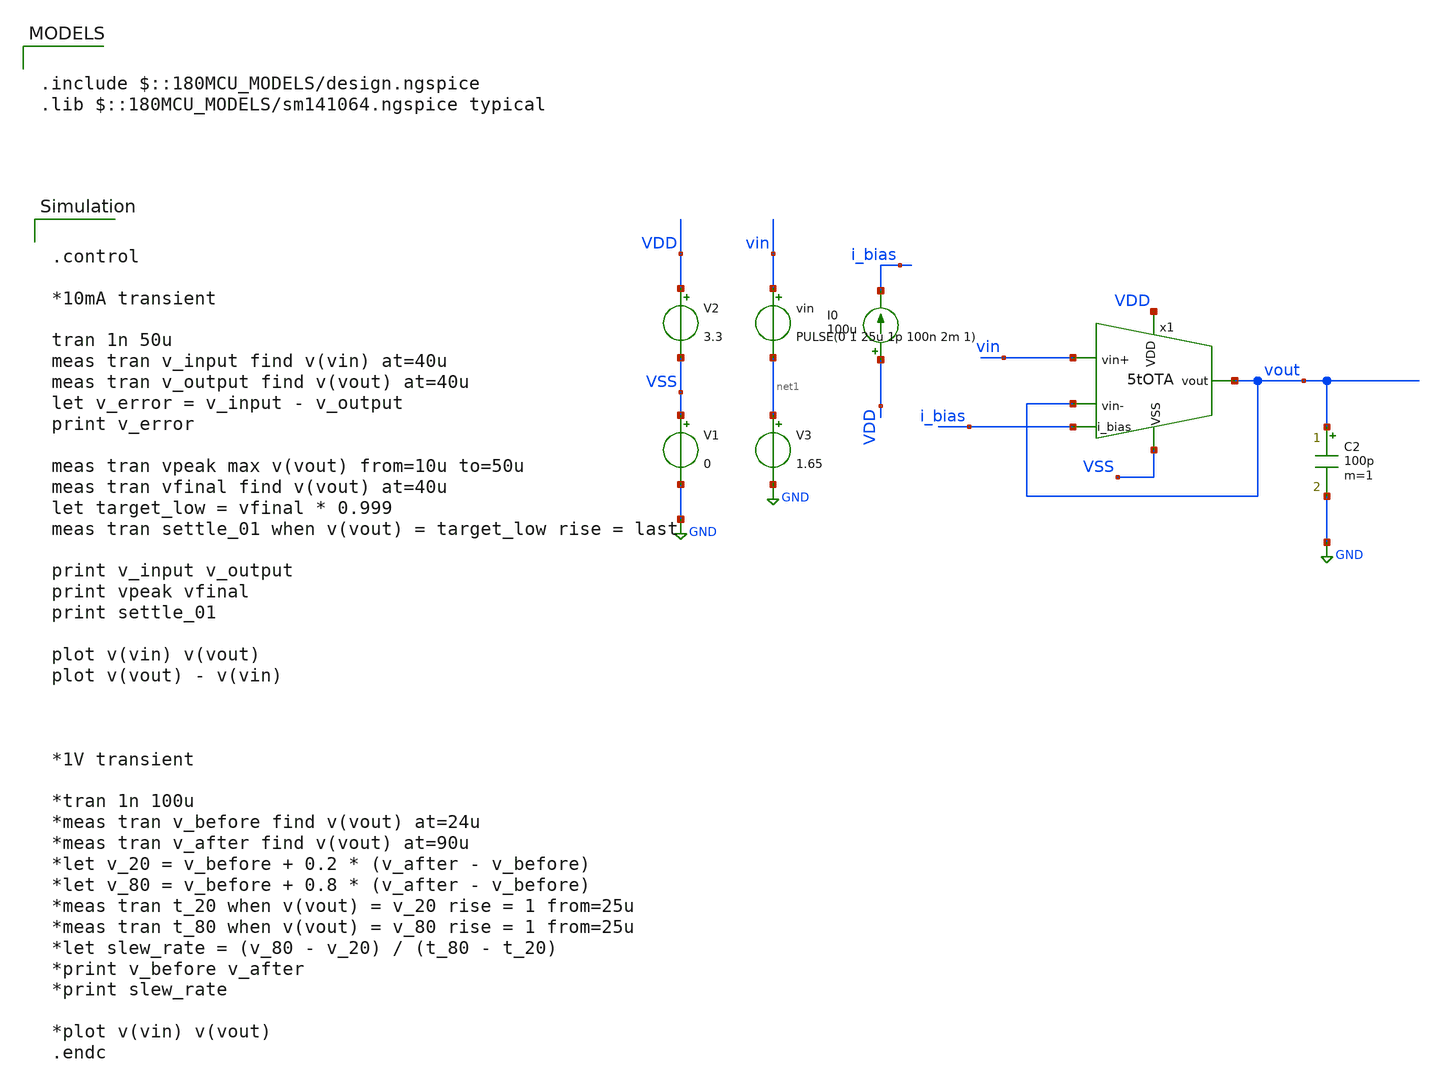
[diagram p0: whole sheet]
** sch_path: designs/5tOTA_tb_tran.sch
**.subckt 5tOTA_tb_tran
x1 VDD vout vin vout i_bias VSS 5tOTA
V1 VSS GND 0
V2 VDD VSS 3.3
I0 VDD i_bias 100u
vin vin net1 PULSE(0 1 25u 1p 100n 2m 1)
C2 vout GND 100p m=1
V3 net1 GND 1.65
**** begin user architecture code

.include $::180MCU_MODELS/design.ngspice
.lib $::180MCU_MODELS/sm141064.ngspice typical



.control

*10mA transient

tran 1n 50u
meas tran v_input find v(vin) at=40u
meas tran v_output find v(vout) at=40u
let v_error = v_input - v_output
print v_error

meas tran vpeak max v(vout) from=10u to=50u
meas tran vfinal find v(vout) at=40u
let target_low = vfinal * 0.999
meas tran settle_01 when v(vout) = target_low rise = last

print v_input v_output
print vpeak vfinal
print settle_01

plot v(vin) v(vout)
plot v(vout) - v(vin)



*1V transient

*tran 1n 100u
*meas tran v_before find v(vout) at=24u
*meas tran v_after find v(vout) at=90u
*let v_20 = v_before + 0.2 * (v_after - v_before)
*let v_80 = v_before + 0.8 * (v_after - v_before)
*meas tran t_20 when v(vout) = v_20 rise = 1 from=25u
*meas tran t_80 when v(vout) = v_80 rise = 1 from=25u
*let slew_rate = (v_80 - v_20) / (t_80 - t_20)
*print v_before v_after
*print slew_rate

*plot v(vin) v(vout)
.endc


**** end user architecture code
**.ends

* expanding   symbol:  5tOTA.sym # of pins=6
** sym_path: designs/5tOTA.sym
** sch_path: designs/5tOTA.sch
.subckt 5tOTA VDD vout vin+ vin- i_bias VSS
*.ipin VDD
*.opin vout
*.ipin i_bias
*.ipin vin+
*.ipin vin-
*.ipin VSS
XM1 net1 vin+ net2 VSS nfet_03v3 L=0.5u W=11.43u nf=1 ad='int((nf+1)/2) * W/nf * 0.18u' as='int((nf+2)/2) * W/nf * 0.18u'
+ pd='2*int((nf+1)/2) * (W/nf + 0.18u)' ps='2*int((nf+2)/2) * (W/nf + 0.18u)' nrd='0.18u / W' nrs='0.18u / W'
+ sa=0 sb=0 sd=0 m=1
XM2 vout vin- net2 VSS nfet_03v3 L=0.5u W=11.43u nf=1 ad='int((nf+1)/2) * W/nf * 0.18u' as='int((nf+2)/2) * W/nf * 0.18u'
+ pd='2*int((nf+1)/2) * (W/nf + 0.18u)' ps='2*int((nf+2)/2) * (W/nf + 0.18u)' nrd='0.18u / W' nrs='0.18u / W'
+ sa=0 sb=0 sd=0 m=1
XM3 net1 net1 VDD VDD pfet_03v3 L=0.5u W=22.86u nf=1 ad='int((nf+1)/2) * W/nf * 0.18u' as='int((nf+2)/2) * W/nf * 0.18u'
+ pd='2*int((nf+1)/2) * (W/nf + 0.18u)' ps='2*int((nf+2)/2) * (W/nf + 0.18u)' nrd='0.18u / W' nrs='0.18u / W'
+ sa=0 sb=0 sd=0 m=1
XM4 vout net1 VDD VDD pfet_03v3 L=0.5u W=22.86u nf=1 ad='int((nf+1)/2) * W/nf * 0.18u' as='int((nf+2)/2) * W/nf * 0.18u'
+ pd='2*int((nf+1)/2) * (W/nf + 0.18u)' ps='2*int((nf+2)/2) * (W/nf + 0.18u)' nrd='0.18u / W' nrs='0.18u / W'
+ sa=0 sb=0 sd=0 m=1
XM5 net2 i_bias VSS VSS nfet_03v3 L=0.5u W=22.86u nf=1 ad='int((nf+1)/2) * W/nf * 0.18u' as='int((nf+2)/2) * W/nf * 0.18u'
+ pd='2*int((nf+1)/2) * (W/nf + 0.18u)' ps='2*int((nf+2)/2) * (W/nf + 0.18u)' nrd='0.18u / W' nrs='0.18u / W'
+ sa=0 sb=0 sd=0 m=1
XM6 i_bias i_bias VSS VSS nfet_03v3 L=0.5u W=22.86u nf=1 ad='int((nf+1)/2) * W/nf * 0.18u' as='int((nf+2)/2) * W/nf * 0.18u'
+ pd='2*int((nf+1)/2) * (W/nf + 0.18u)' ps='2*int((nf+2)/2) * (W/nf + 0.18u)' nrd='0.18u / W' nrs='0.18u / W'
+ sa=0 sb=0 sd=0 m=1
.ends

.GLOBAL GND
.end
